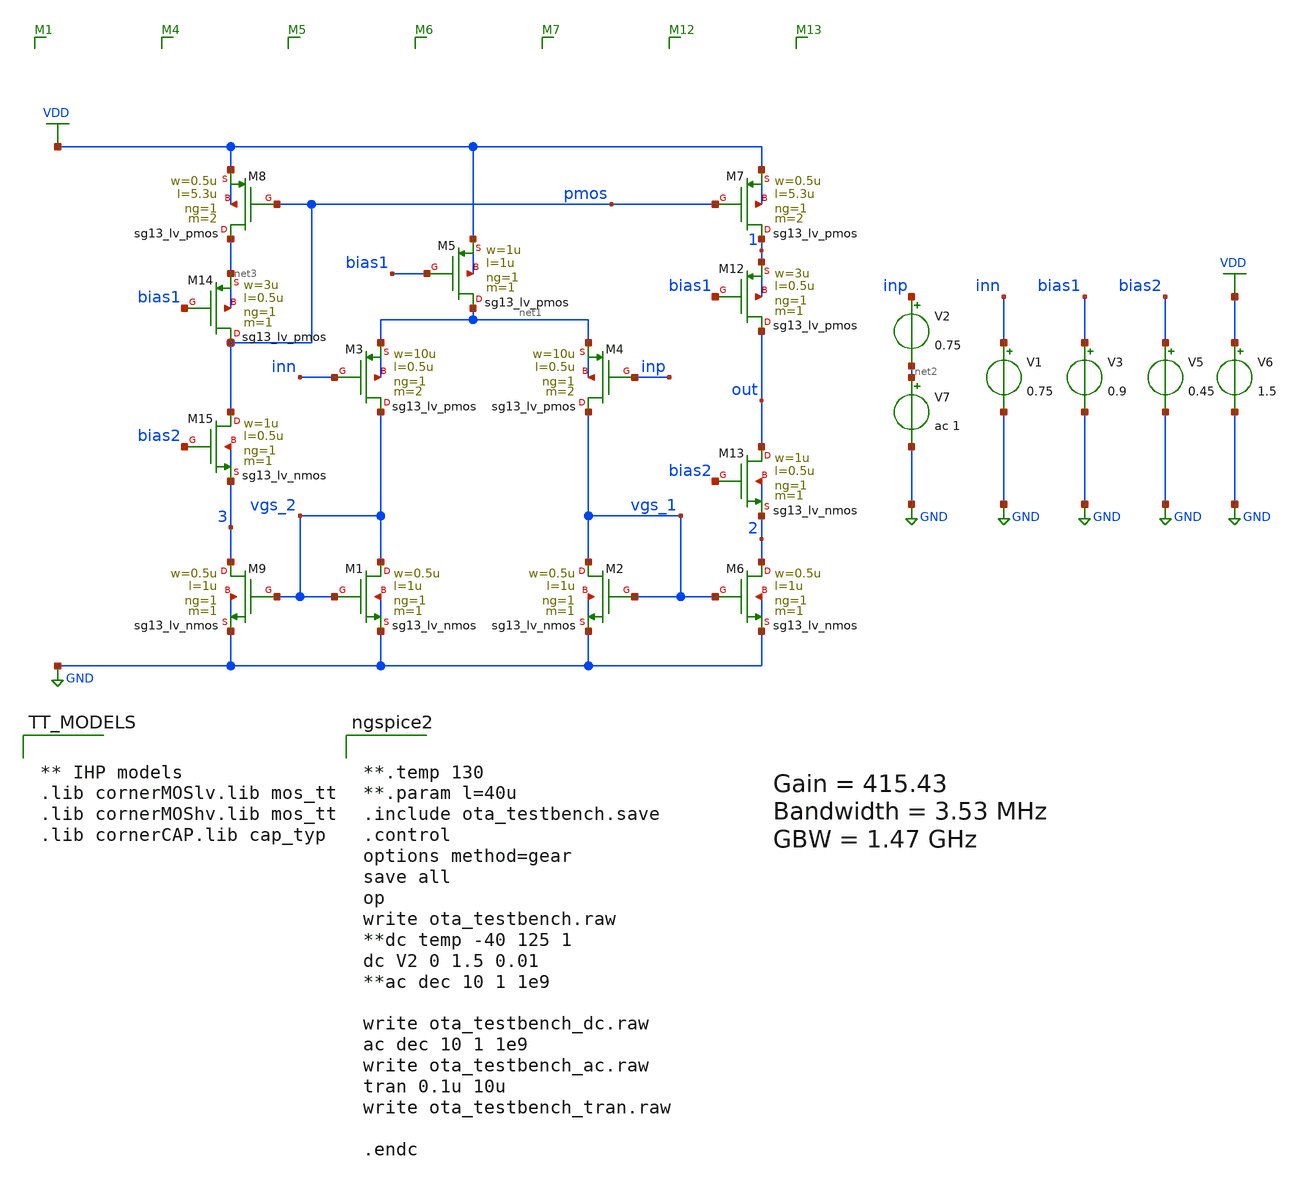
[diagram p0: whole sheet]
** sch_path: ota/ota_testbench.sch
**.subckt ota_testbench
XM1 vgs_2 vgs_2 GND GND sg13_lv_nmos w=0.5u l=1u ng=1 m=1 mm_ok=1
XM3 vgs_2 inn net1 net1 sg13_lv_pmos w=10u l=0.5u ng=1 m=2 mm_ok=1
XM4 vgs_1 inp net1 net1 sg13_lv_pmos w=10u l=0.5u ng=1 m=2 mm_ok=1
XM2 vgs_1 vgs_1 GND GND sg13_lv_nmos w=0.5u l=1u ng=1 m=1 mm_ok=1
XM5 net1 bias1 VDD VDD sg13_lv_pmos w=1u l=1u ng=1 m=1 mm_ok=1
XM6 2 vgs_1 GND GND sg13_lv_nmos w=0.5u l=1u ng=1 m=1 mm_ok=1
XM7 1 pmos VDD VDD sg13_lv_pmos w=0.5u l=5.3u ng=1 m=2 mm_ok=1
XM8 net3 pmos VDD VDD sg13_lv_pmos w=0.5u l=5.3u ng=1 m=2 mm_ok=1
XM9 3 vgs_2 GND GND sg13_lv_nmos w=0.5u l=1u ng=1 m=1 mm_ok=1
V3 bias1 GND 0.9
V1 inn GND 0.75
V2 inp net2 0.75
V6 VDD GND 1.5
V7 net2 GND ac 1
XM12 out bias1 1 1 sg13_lv_pmos w=3u l=0.5u ng=1 m=1 mm_ok=1
XM13 out bias2 2 2 sg13_lv_nmos w=1u l=0.5u ng=1 m=1 mm_ok=1
XM14 pmos bias1 net3 net3 sg13_lv_pmos w=3u l=0.5u ng=1 m=1 mm_ok=1
XM15 pmos bias2 3 3 sg13_lv_nmos w=1u l=0.5u ng=1 m=1 mm_ok=1
V5 bias2 GND 0.45
**** begin user architecture code


** IHP models
.lib cornerMOSlv.lib mos_tt
.lib cornerMOShv.lib mos_tt
.lib cornerCAP.lib cap_typ




**.temp 130
**.param l=40u
.include ota_testbench.save
.control
options method=gear
save all
op
write ota_testbench.raw
**dc temp -40 125 1
dc V2 0 1.5 0.01
**ac dec 10 1 1e9

write ota_testbench_dc.raw
ac dec 10 1 1e9
write ota_testbench_ac.raw
tran 0.1u 10u
write ota_testbench_tran.raw

.endc


Gain =
**** end user architecture code
**.ends
.GLOBAL GND
.GLOBAL VDD
.end
